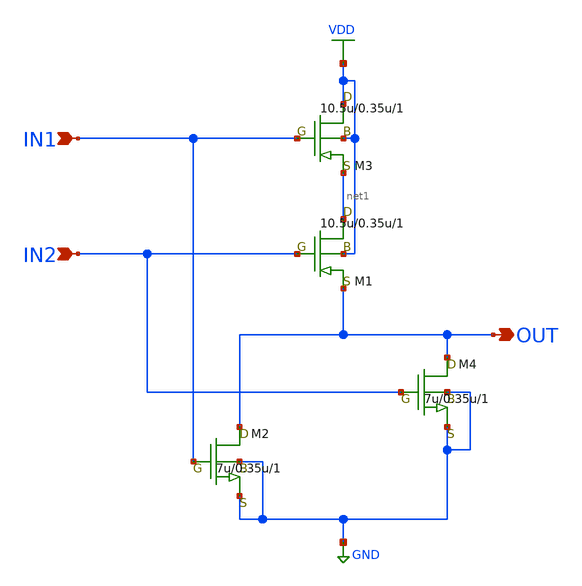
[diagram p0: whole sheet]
** sch_path: LR_hasegawa/LR_Work2/NOR2.sch
**.subckt NOR2 IN1 IN2 OUT
*.ipin IN1
*.ipin IN2
*.opin OUT
M1 net1 IN2 OUT VDD pch w=10.5u l=0.35u as=0 ps=0 ad=0 pd=0 m=1
M2 OUT IN1 GND GND nch w=7u l=0.35u as=0 ps=0 ad=0 pd=0 m=1
M3 VDD IN1 net1 VDD pch w=10.5u l=0.35u as=0 ps=0 ad=0 pd=0 m=1
M4 OUT IN2 GND GND nch w=7u l=0.35u as=0 ps=0 ad=0 pd=0 m=1
**.ends
.GLOBAL VDD
.GLOBAL GND
.end
